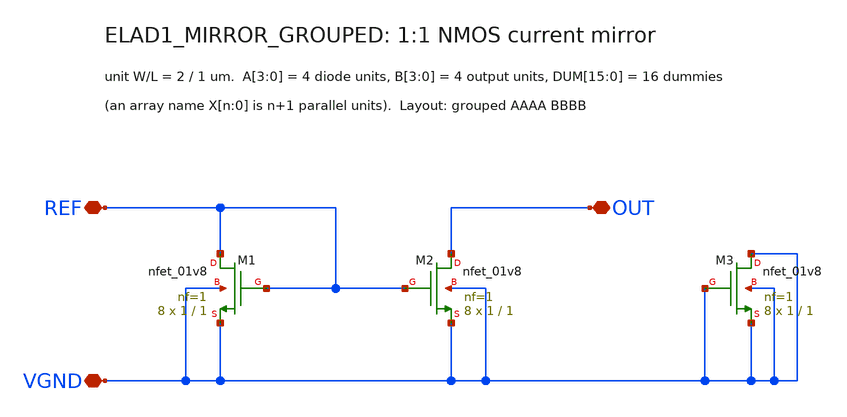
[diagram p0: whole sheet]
** sch_path: cells/ELAD1_MIRROR_GROUPED/schematic/ELAD1_MIRROR_GROUPED.sch
**.subckt ELAD1_MIRROR_GROUPED REF OUT VGND
*.iopin REF
*.iopin OUT
*.iopin VGND
XM1 REF REF VGND VGND sky130_fd_pr__nfet_01v8 L=1 W=1 nf=1 ad='int((1 + 1)/2) * 1 / 1 * 0.29' as='int((1 + 2)/2) * 1 / 1 * 0.29'
+ pd='2*int((1 + 1)/2) * (1 / 1 + 0.29)' ps='2*int((1 + 2)/2) * (1 / 1 + 0.29)' nrd='0.29 / 1 ' nrs='0.29 / 1 '
+ sa=0 sb=0 sd=0 mult=8 m=8
XM2 OUT REF VGND VGND sky130_fd_pr__nfet_01v8 L=1 W=1 nf=1 ad='int((1 + 1)/2) * 1 / 1 * 0.29' as='int((1 + 2)/2) * 1 / 1 * 0.29'
+ pd='2*int((1 + 1)/2) * (1 / 1 + 0.29)' ps='2*int((1 + 2)/2) * (1 / 1 + 0.29)' nrd='0.29 / 1 ' nrs='0.29 / 1 '
+ sa=0 sb=0 sd=0 mult=8 m=8
XM3 VGND VGND VGND VGND sky130_fd_pr__nfet_01v8 L=1 W=1 nf=1 ad='int((1 + 1)/2) * 1 / 1 * 0.29' as='int((1 + 2)/2) * 1 / 1 * 0.29'
+ pd='2*int((1 + 1)/2) * (1 / 1 + 0.29)' ps='2*int((1 + 2)/2) * (1 / 1 + 0.29)' nrd='0.29 / 1 ' nrs='0.29 / 1 '
+ sa=0 sb=0 sd=0 mult=8 m=8
**.ends
.end
